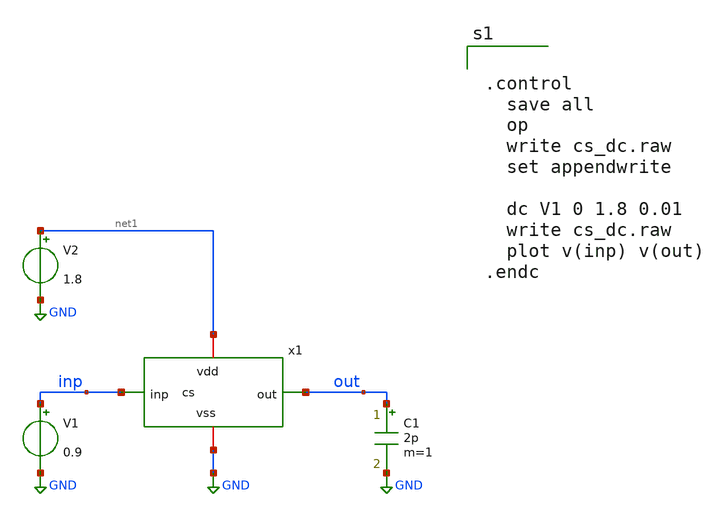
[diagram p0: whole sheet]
** sch_path: xschem/cs_dc.sch
**.subckt cs_dc
x1 out inp net1 GND cs
V1 inp GND 0.9
V2 net1 GND 1.8
C1 out GND 2p m=1
**** begin user architecture code

** opencircuitdesign pdks install
.lib $::SKYWATER_MODELS/sky130.lib.spice tt




.control
  save all
  op
  write cs_dc.raw
  set appendwrite

  dc V1 0 1.8 0.01
  write cs_dc.raw
  plot v(inp) v(out)
.endc


**** end user architecture code
**.ends

* expanding   symbol:  cs.sym # of pins=4
** sym_path: xschem/cs.sym
.include cs_pex.spice
.GLOBAL GND
.end
